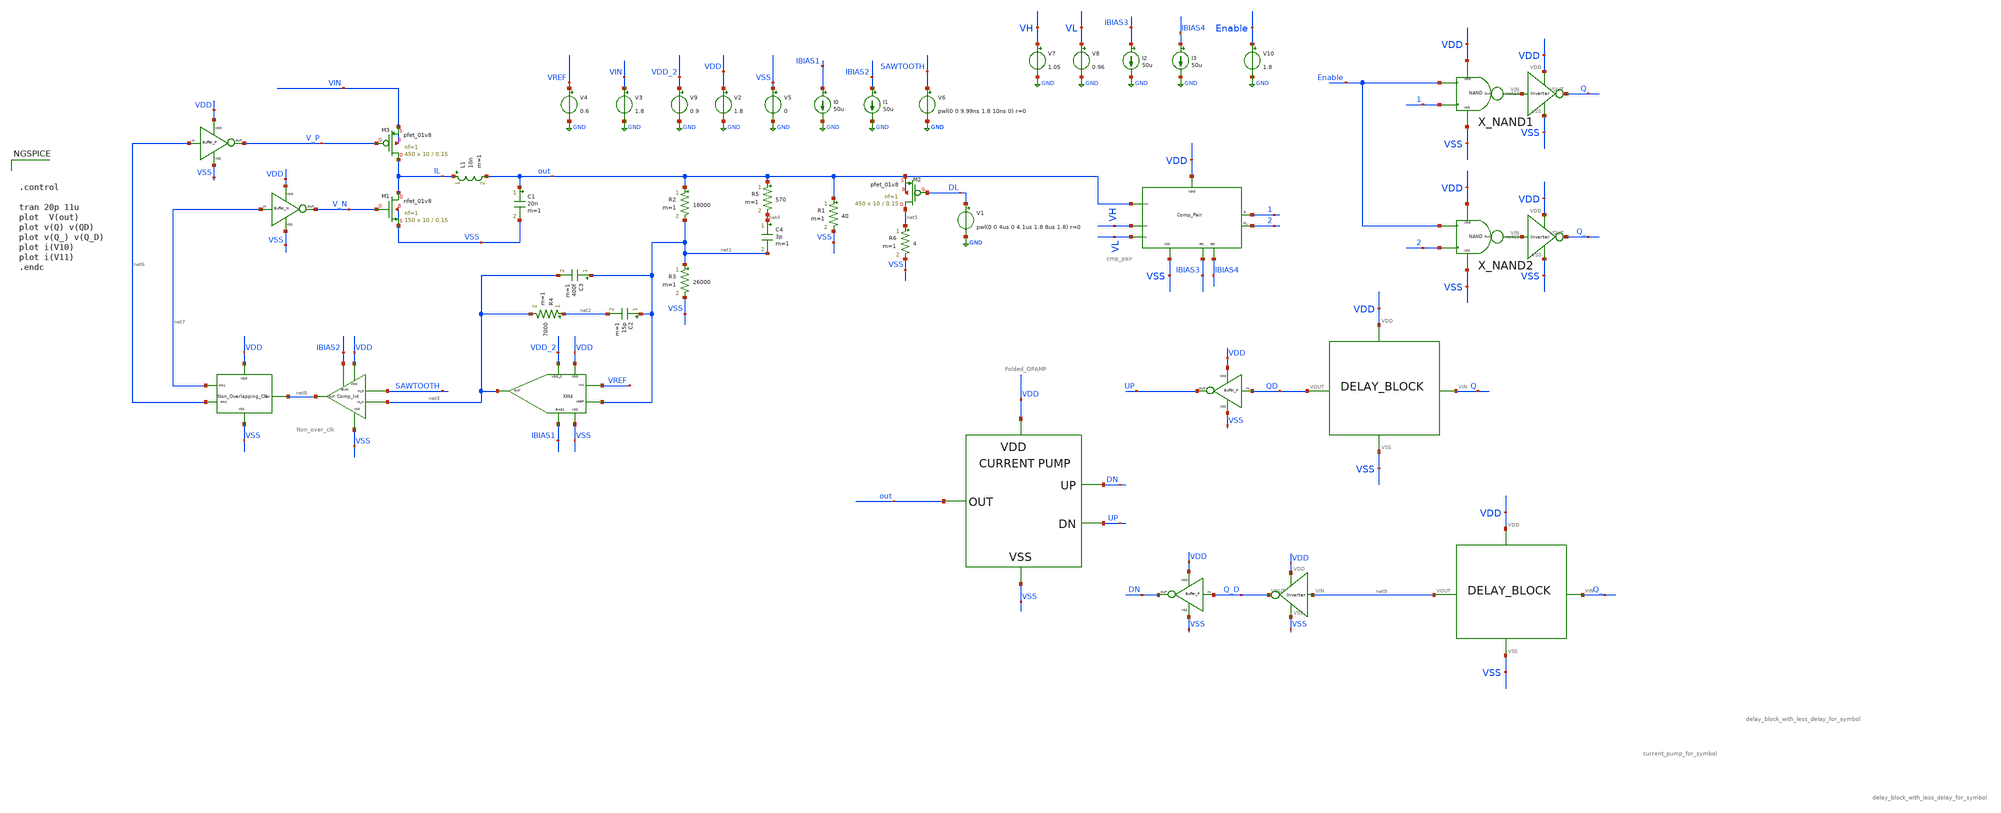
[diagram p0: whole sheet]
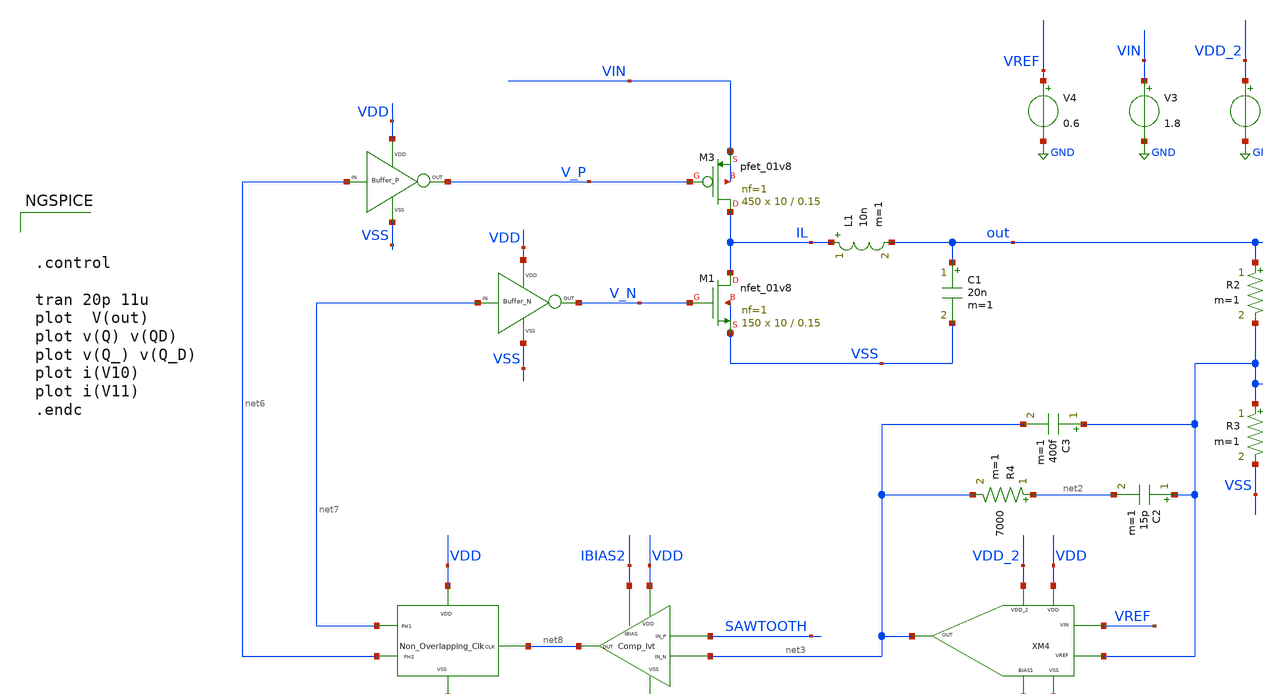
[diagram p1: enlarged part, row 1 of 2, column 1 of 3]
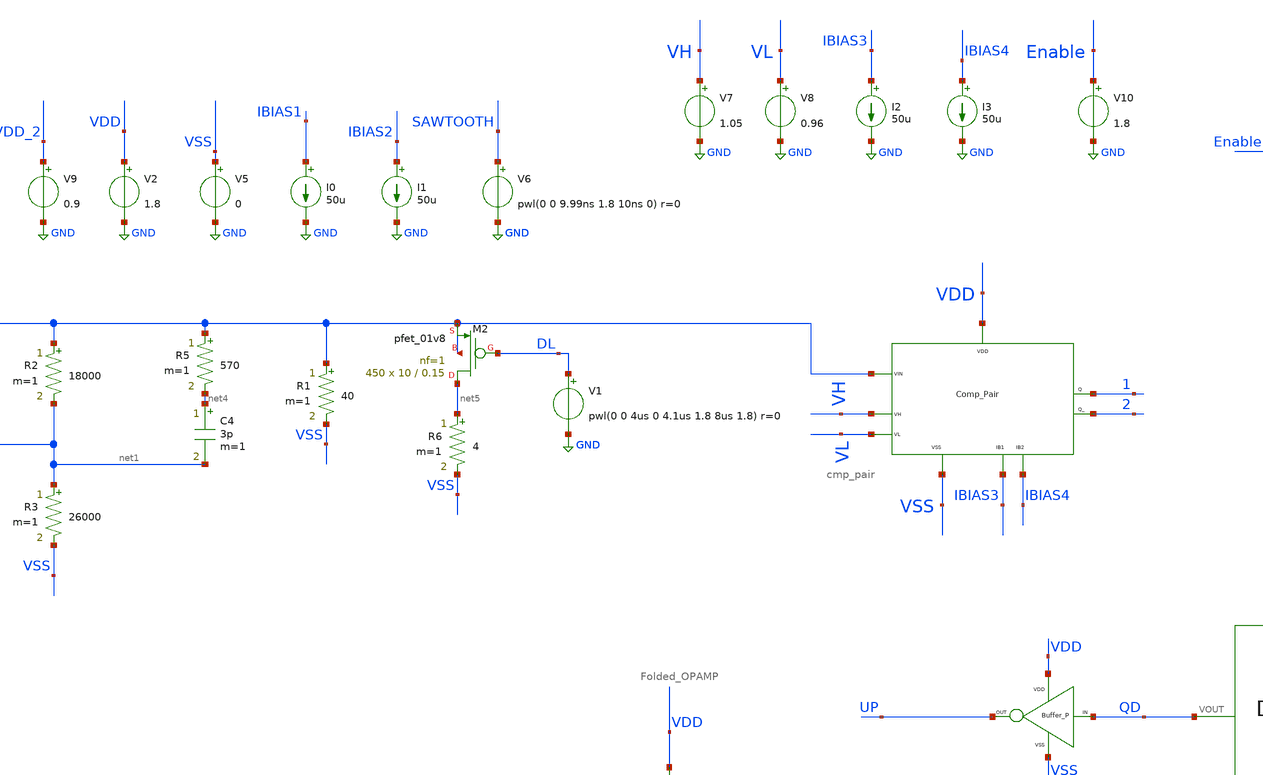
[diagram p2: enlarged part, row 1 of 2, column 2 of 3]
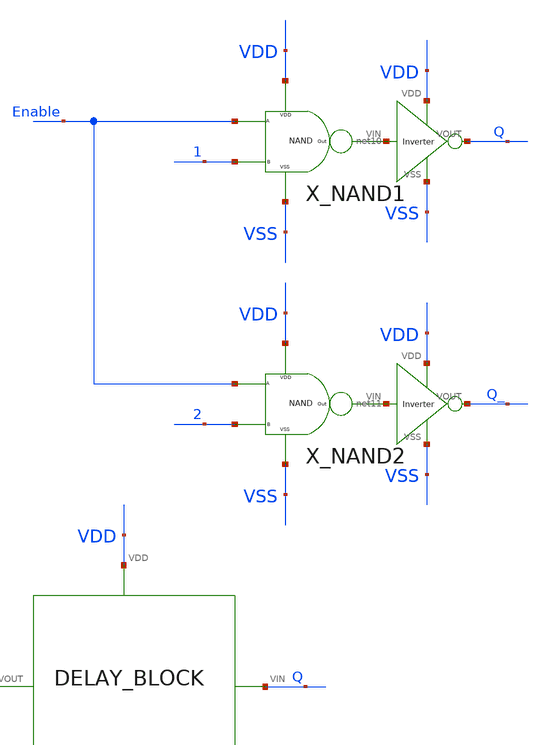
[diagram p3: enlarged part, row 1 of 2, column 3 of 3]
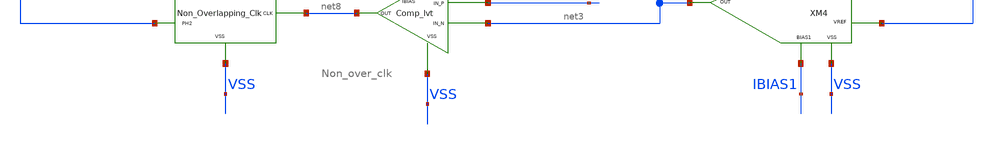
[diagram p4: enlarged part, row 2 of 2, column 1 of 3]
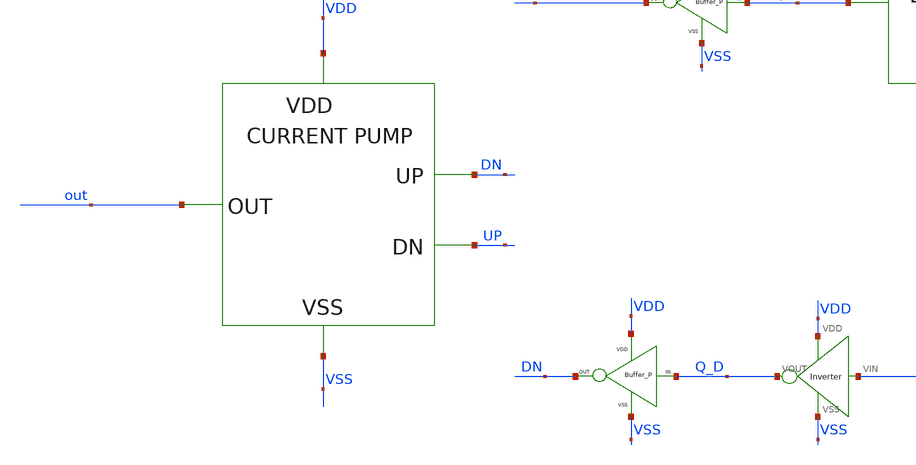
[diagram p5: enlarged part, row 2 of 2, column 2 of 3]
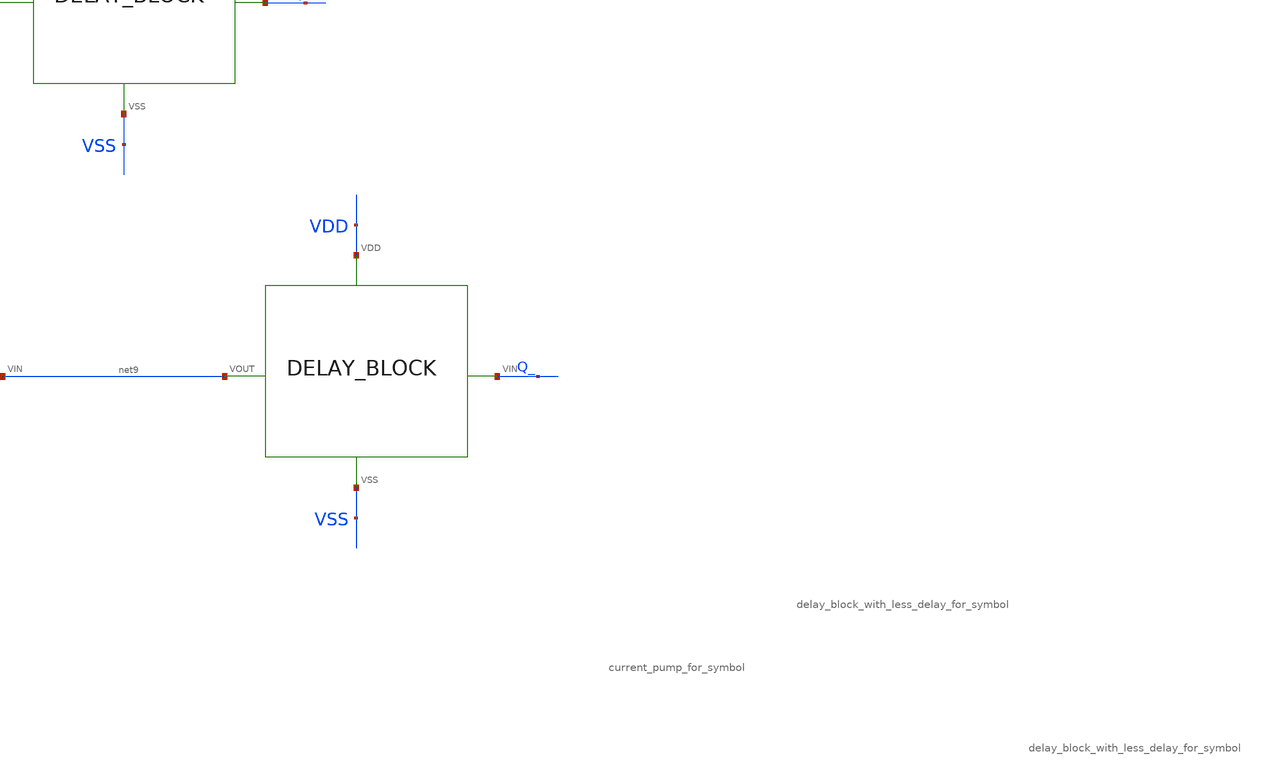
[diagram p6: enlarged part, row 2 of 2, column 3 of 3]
** sch_path: xschem/DC_DC_Converter_xschem/OTHERS/DC_DC_Converter_2/DC_DC_Converter/TOP_LEVEL/closed_loop_v8.sch
**.subckt closed_loop_v8
XM3 IL V_P VIN VIN sky130_fd_pr__pfet_01v8 L=0.15 W=10 nf=1 ad='int((nf+1)/2) * W/nf * 0.29' as='int((nf+2)/2) * W/nf * 0.29'
+ pd='2*int((nf+1)/2) * (W/nf + 0.29)' ps='2*int((nf+2)/2) * (W/nf + 0.29)' nrd='0.29 / W' nrs='0.29 / W'
+ sa=0 sb=0 sd=0 mult=450 m=450
L1 IL out 10n m=1
C1 out VSS 20n m=1
V3 VIN GND 1.8
I0 IBIAS1 GND 50u
V9 VDD_2 GND 0.9
V2 VDD GND 1.8
V5 VSS GND 0
V4 VREF GND 0.6
I1 IBIAS2 GND 50u
V6 SAWTOOTH GND pwl(0 0 9.99ns 1.8 10ns 0) r=0
R2 out net1 18000 m=1
R3 net1 VSS 26000 m=1
R4 net2 net3 7000 m=1
C2 net1 net2 15p m=1
C3 net1 net3 400f m=1
R5 out net4 570 m=1
C4 net4 net1 3p m=1
R1 out VSS 40 m=1
XM1 IL V_N VSS VSS sky130_fd_pr__nfet_01v8 L=0.15 W=10 nf=1 ad='int((nf+1)/2) * W/nf * 0.29' as='int((nf+2)/2) * W/nf * 0.29'
+ pd='2*int((nf+1)/2) * (W/nf + 0.29)' ps='2*int((nf+2)/2) * (W/nf + 0.29)' nrd='0.29 / W' nrs='0.29 / W'
+ sa=0 sb=0 sd=0 mult=150 m=150
XM2 net5 DL out out sky130_fd_pr__pfet_01v8 L=0.15 W=10 nf=1 ad='int((nf+1)/2) * W/nf * 0.29' as='int((nf+2)/2) * W/nf * 0.29'
+ pd='2*int((nf+1)/2) * (W/nf + 0.29)' ps='2*int((nf+2)/2) * (W/nf + 0.29)' nrd='0.29 / W' nrs='0.29 / W'
+ sa=0 sb=0 sd=0 mult=450 m=450
R6 net5 VSS 4 m=1
V1 DL GND pwl(0 0 4us 0 4.1us 1.8 8us 1.8) r=0
X1 net6 V_P VDD VSS BUFFER_P
X2 net7 V_N VDD VSS BUFFER_N
XM3 net8 VDD VSS net7 net6 Non_over_clk
XM4 VDD VSS VDD_2 IBIAS1 net3 VREF net1 Folded_OPAMP
XM2 IBIAS2 VDD SAWTOOTH net3 VSS net8 Comp_lvt
V7 VH GND 1.05
V8 VL GND 0.96
I2 IBIAS3 GND 50u
I3 IBIAS4 GND 50u
XM1 VDD VSS out VH VL IBIAS3 IBIAS4 1 2 cmp_pair
X3 Q QD VDD VSS delay_block_with_less_delay_for_symbol
X4 Q_ net9 VDD VSS delay_block_with_less_delay_for_symbol
X5 QD UP VDD VSS BUFFER_P
X6 Q_D DN VDD VSS BUFFER_P
X7 DN out VDD VSS UP current_pump_for_symbol
X8 VSS VDD net9 Q_D Inverter
X_NAND1 VDD VSS Enable 1 net10 NAND
X_NAND2 VDD VSS Enable 2 net11 NAND
X9 VSS VDD net10 Q Inverter
X10 VSS VDD net11 Q_ Inverter
V10 Enable GND 1.8
**** begin user architecture code

** opencircuitdesign pdks install
.lib $::SKYWATER_MODELS/sky130.lib.spice tt





.control

tran 20p 11u
plot  V(out)
plot v(Q) v(QD)
plot v(Q_) v(Q_D)
plot i(V10)
plot i(V11)
.endc


**** end user architecture code
**.ends
.GLOBAL GND
.end
